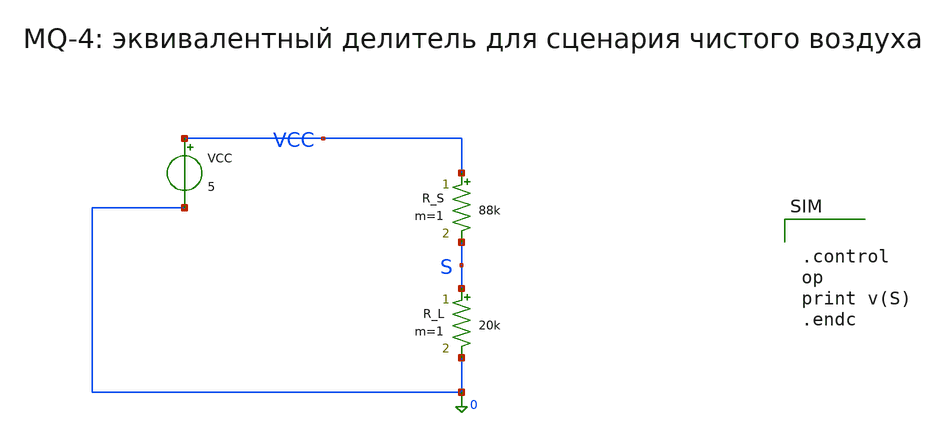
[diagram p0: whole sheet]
** sch_path: docs/figures/xschem_probe/mq4_divider.sch
**.subckt mq4_divider
VCC VCC 0 5
R_S VCC S 88k m=1
R_L S 0 20k m=1
**** begin user architecture code


.control
op
print v(S)
.endc

**** end user architecture code
**.ends
.end
